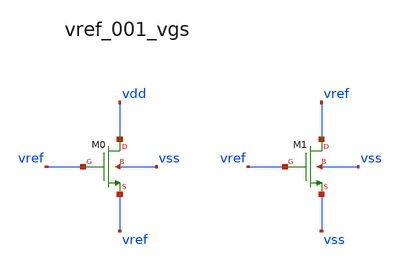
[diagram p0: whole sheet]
** sch_path: analog-db/raw/vref_001_vgs/hier/vref_001_vgs.sch
**.subckt vref_001_vgs
XM0 vdd vref vref vss sg13_lv_nmos w=x_dut_xm0_w l=x_dut_xm0_l ng=1 m=x_dut_xm0_m
XM1 vref vref vss vss sg13_hv_nmos w=x_dut_xm1_w l=x_dut_xm1_l ng=1 m=x_dut_xm1_m
**.ends
.end
